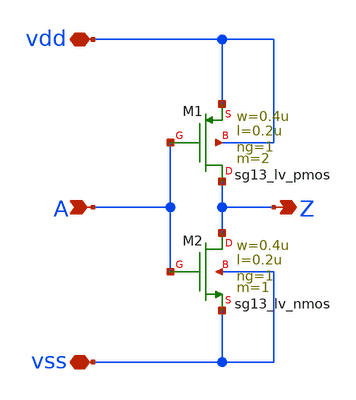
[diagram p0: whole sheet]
** sch_path: v2_feature_extr/inv_tgate.sch
**.subckt inv_tgate A vdd vss Z
*.ipin A
*.iopin vdd
*.iopin vss
*.opin Z
XM1 Z A vdd vdd sg13_lv_pmos w=0.4u l=0.2u ng=1 m=2 mm_ok=1
XM2 Z A vss vss sg13_lv_nmos w=0.4u l=0.2u ng=1 m=1 mm_ok=1
**.ends
.end
